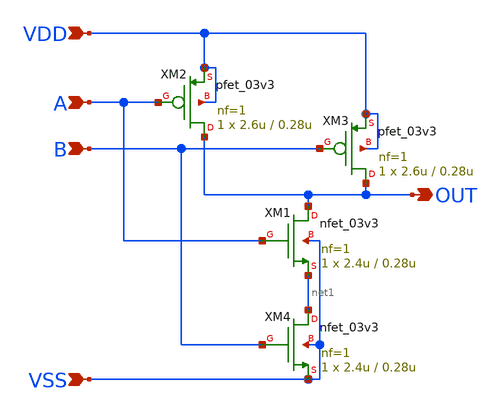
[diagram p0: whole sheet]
** sch_path: Project/1-on-chip/schematic/PNgen/nand_2_out.sch
**.subckt nand_2_out VDD OUT A B VSS
*.ipin VDD
*.opin OUT
*.ipin A
*.ipin B
*.ipin VSS
XM1 OUT A net1 VSS nfet_03v3 L=0.28u W=2.4u nf=1 ad='int((nf+1)/2) * W/nf * 0.18u' as='int((nf+2)/2) * W/nf * 0.18u'
+ pd='2*int((nf+1)/2) * (W/nf + 0.18u)' ps='2*int((nf+2)/2) * (W/nf + 0.18u)' nrd='0.18u / W' nrs='0.18u / W'
+ sa=0 sb=0 sd=0 m=1
XM2 OUT A VDD VDD pfet_03v3 L=0.28u W=2.6u nf=1 ad='int((nf+1)/2) * W/nf * 0.18u' as='int((nf+2)/2) * W/nf * 0.18u'
+ pd='2*int((nf+1)/2) * (W/nf + 0.18u)' ps='2*int((nf+2)/2) * (W/nf + 0.18u)' nrd='0.18u / W' nrs='0.18u / W'
+ sa=0 sb=0 sd=0 m=1
XM3 OUT B VDD VDD pfet_03v3 L=0.28u W=2.6u nf=1 ad='int((nf+1)/2) * W/nf * 0.18u' as='int((nf+2)/2) * W/nf * 0.18u'
+ pd='2*int((nf+1)/2) * (W/nf + 0.18u)' ps='2*int((nf+2)/2) * (W/nf + 0.18u)' nrd='0.18u / W' nrs='0.18u / W'
+ sa=0 sb=0 sd=0 m=1
XM4 net1 B VSS VSS nfet_03v3 L=0.28u W=2.4u nf=1 ad='int((nf+1)/2) * W/nf * 0.18u' as='int((nf+2)/2) * W/nf * 0.18u'
+ pd='2*int((nf+1)/2) * (W/nf + 0.18u)' ps='2*int((nf+2)/2) * (W/nf + 0.18u)' nrd='0.18u / W' nrs='0.18u / W'
+ sa=0 sb=0 sd=0 m=1
**.ends
.end
